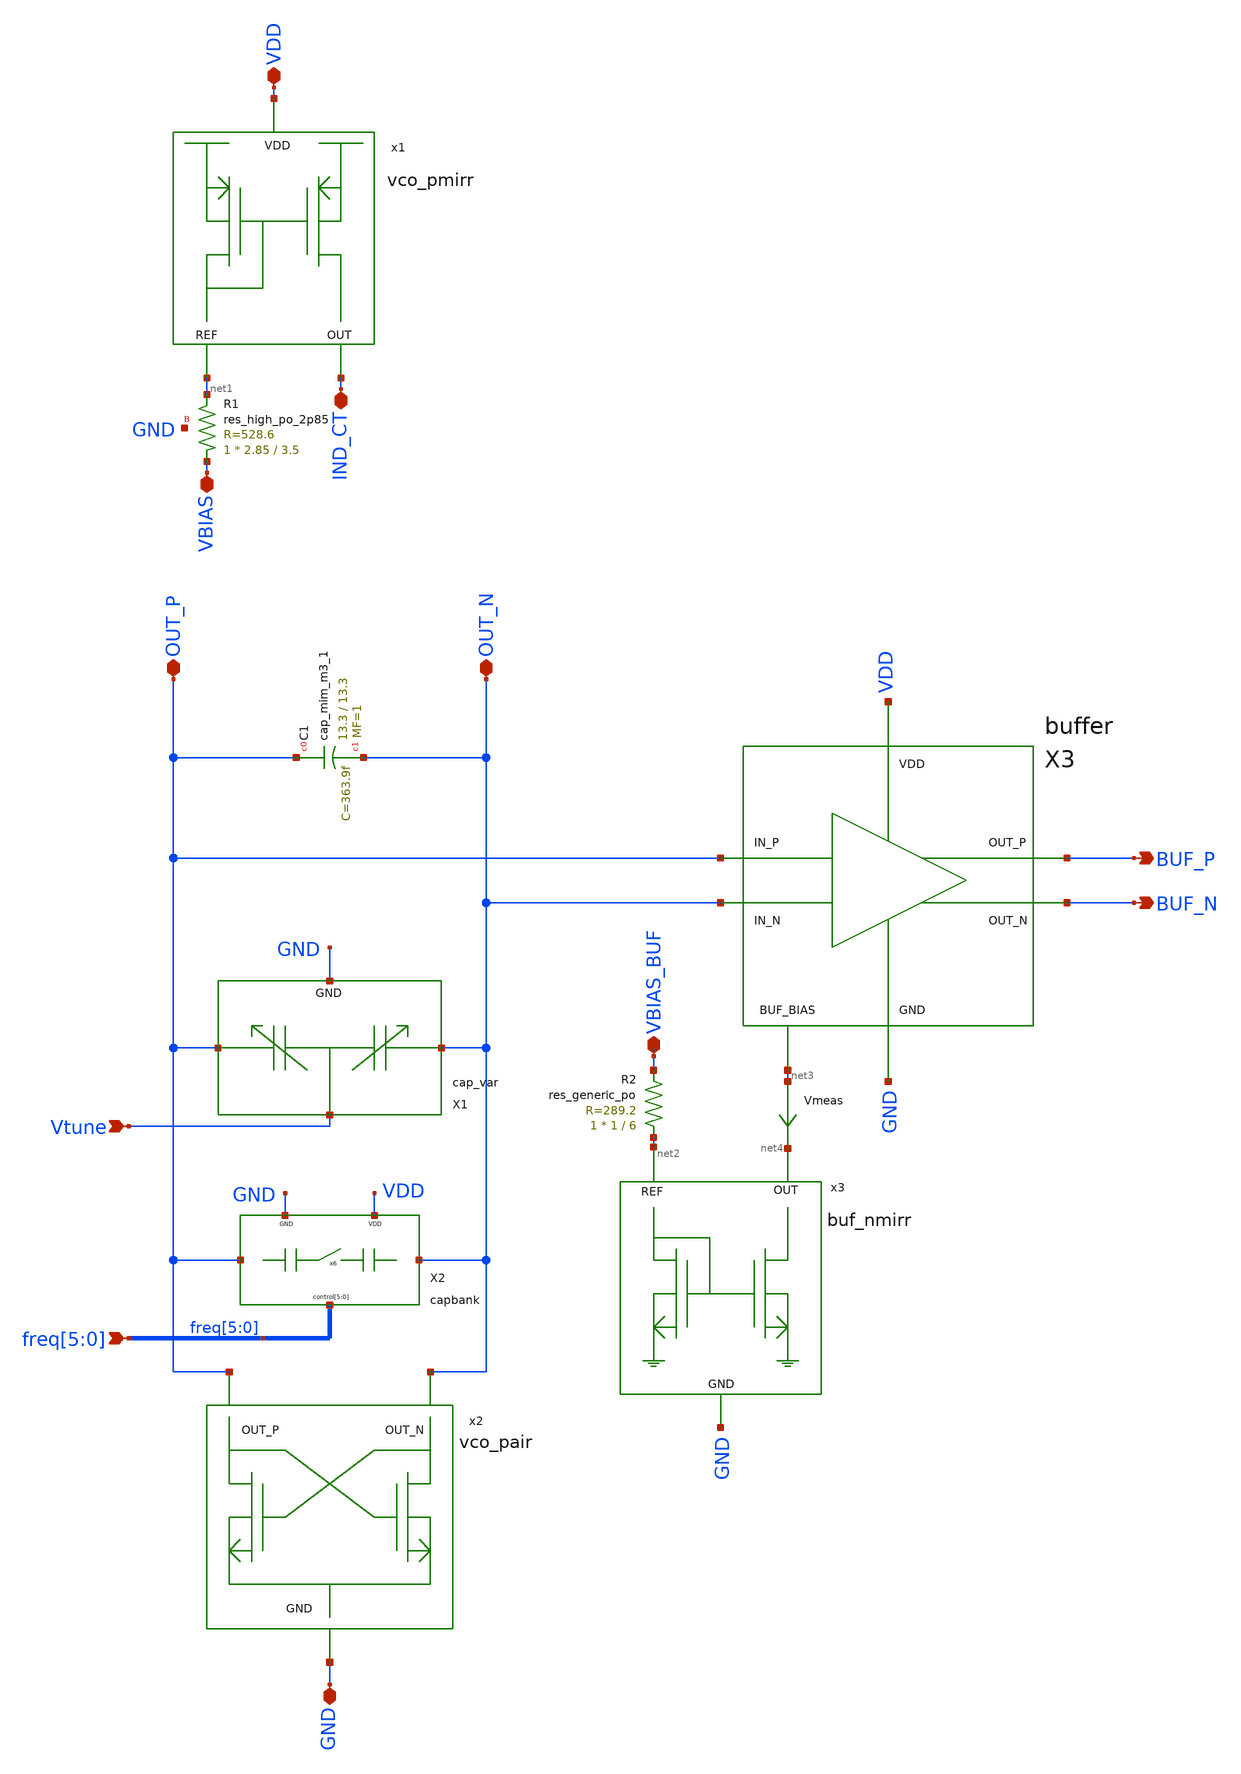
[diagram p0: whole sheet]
** sch_path: xschem/vco/parts/vco_wo_ind.sch
**.subckt vco_wo_ind OUT_P IND_CT GND BUF_P BUF_N OUT_N VBIAS_BUF VDD VBIAS
*+ freq[5],freq[4],freq[3],freq[2],freq[1],freq[0] Vtune
*.iopin OUT_P
*.iopin IND_CT
*.iopin GND
*.opin BUF_P
*.opin BUF_N
*.iopin OUT_N
*.iopin VBIAS_BUF
*.iopin VDD
*.iopin VBIAS
*.ipin freq[5],freq[4],freq[3],freq[2],freq[1],freq[0]
*.ipin Vtune
X1 OUT_P OUT_N GND Vtune cap_var
X2 OUT_P OUT_N VDD freq[5] freq[4] freq[3] freq[2] freq[1] freq[0] GND capbank
XC1 OUT_P OUT_N sky130_fd_pr__cap_mim_m3_1 W=13.3 L=13.3 MF=1 m=1
XR2 net2 VBIAS_BUF sky130_fd_pr__res_generic_po W=1 L=6 m=1
x1 VDD IND_CT net1 vco_pmirr
x2 OUT_P OUT_N GND vco_pair
X3 net3 VDD GND BUF_N BUF_P OUT_P OUT_N buffer
x3 net2 net4 GND buf_nmirr
XR1 VBIAS net1 GND sky130_fd_pr__res_high_po_2p85 L=3.5 mult=1 m=1
Vmeas net3 net4 0
.save i(vmeas)
**.ends
.end
